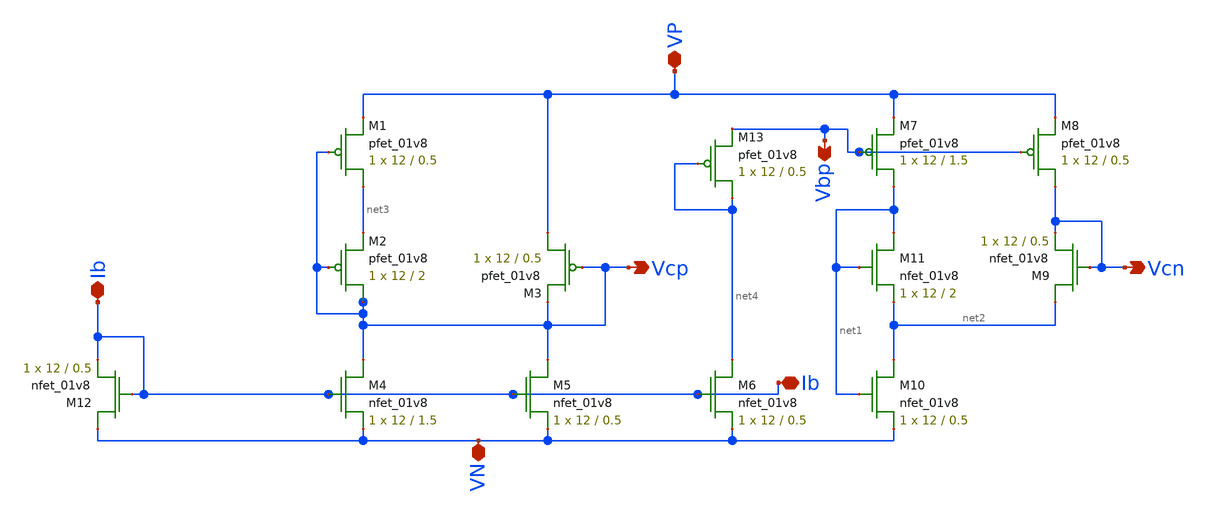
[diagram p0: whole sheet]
** sch_path: mp3/schematic/bias.sch
**.subckt bias VP VN Vcp Vcn Vbp Ib Ib
*.iopin VP
*.iopin VN
*.opin Vcp
*.opin Vcn
*.opin Vbp
*.iopin Ib
*.iopin Ib
XM1 net3 Vcp VP VDD sky130_fd_pr__pfet_01v8 L=0.5 W=12 nf=1 ad='int((nf+1)/2) * W/nf * 0.29' as='int((nf+2)/2) * W/nf * 0.29'
+ pd='2*int((nf+1)/2) * (W/nf + 0.29)' ps='2*int((nf+2)/2) * (W/nf + 0.29)' nrd='0.29 / W' nrs='0.29 / W'
+ sa=0 sb=0 sd=0 mult=1 m=1
XM2 Vcp Vcp net3 VDD sky130_fd_pr__pfet_01v8 L=2 W=12 nf=1 ad='int((nf+1)/2) * W/nf * 0.29' as='int((nf+2)/2) * W/nf * 0.29'
+ pd='2*int((nf+1)/2) * (W/nf + 0.29)' ps='2*int((nf+2)/2) * (W/nf + 0.29)' nrd='0.29 / W' nrs='0.29 / W'
+ sa=0 sb=0 sd=0 mult=1 m=1
XM3 VP Vcp Vcp VDD sky130_fd_pr__pfet_01v8 L=0.5 W=12 nf=1 ad='int((nf+1)/2) * W/nf * 0.29' as='int((nf+2)/2) * W/nf * 0.29'
+ pd='2*int((nf+1)/2) * (W/nf + 0.29)' ps='2*int((nf+2)/2) * (W/nf + 0.29)' nrd='0.29 / W' nrs='0.29 / W'
+ sa=0 sb=0 sd=0 mult=1 m=1
XM4 Vcp Ib VN GND sky130_fd_pr__nfet_01v8 L=1.5 W=12 nf=1 ad='int((nf+1)/2) * W/nf * 0.29' as='int((nf+2)/2) * W/nf * 0.29'
+ pd='2*int((nf+1)/2) * (W/nf + 0.29)' ps='2*int((nf+2)/2) * (W/nf + 0.29)' nrd='0.29 / W' nrs='0.29 / W'
+ sa=0 sb=0 sd=0 mult=1 m=1
XM5 Vcp Ib VN GND sky130_fd_pr__nfet_01v8 L=0.5 W=12 nf=1 ad='int((nf+1)/2) * W/nf * 0.29' as='int((nf+2)/2) * W/nf * 0.29'
+ pd='2*int((nf+1)/2) * (W/nf + 0.29)' ps='2*int((nf+2)/2) * (W/nf + 0.29)' nrd='0.29 / W' nrs='0.29 / W'
+ sa=0 sb=0 sd=0 mult=1 m=1
XM6 net4 Ib VN GND sky130_fd_pr__nfet_01v8 L=0.5 W=12 nf=1 ad='int((nf+1)/2) * W/nf * 0.29' as='int((nf+2)/2) * W/nf * 0.29'
+ pd='2*int((nf+1)/2) * (W/nf + 0.29)' ps='2*int((nf+2)/2) * (W/nf + 0.29)' nrd='0.29 / W' nrs='0.29 / W'
+ sa=0 sb=0 sd=0 mult=1 m=1
XM7 net1 Vbp VP VDD sky130_fd_pr__pfet_01v8 L=1.5 W=12 nf=1 ad='int((nf+1)/2) * W/nf * 0.29' as='int((nf+2)/2) * W/nf * 0.29'
+ pd='2*int((nf+1)/2) * (W/nf + 0.29)' ps='2*int((nf+2)/2) * (W/nf + 0.29)' nrd='0.29 / W' nrs='0.29 / W'
+ sa=0 sb=0 sd=0 mult=1 m=1
XM8 Vcn Vbp VP VDD sky130_fd_pr__pfet_01v8 L=0.5 W=12 nf=1 ad='int((nf+1)/2) * W/nf * 0.29' as='int((nf+2)/2) * W/nf * 0.29'
+ pd='2*int((nf+1)/2) * (W/nf + 0.29)' ps='2*int((nf+2)/2) * (W/nf + 0.29)' nrd='0.29 / W' nrs='0.29 / W'
+ sa=0 sb=0 sd=0 mult=1 m=1
XM9 net2 Vcn Vcn GND sky130_fd_pr__nfet_01v8 L=0.5 W=12 nf=1 ad='int((nf+1)/2) * W/nf * 0.29' as='int((nf+2)/2) * W/nf * 0.29'
+ pd='2*int((nf+1)/2) * (W/nf + 0.29)' ps='2*int((nf+2)/2) * (W/nf + 0.29)' nrd='0.29 / W' nrs='0.29 / W'
+ sa=0 sb=0 sd=0 mult=1 m=1
XM10 net2 net1 VN GND sky130_fd_pr__nfet_01v8 L=0.5 W=12 nf=1 ad='int((nf+1)/2) * W/nf * 0.29' as='int((nf+2)/2) * W/nf * 0.29'
+ pd='2*int((nf+1)/2) * (W/nf + 0.29)' ps='2*int((nf+2)/2) * (W/nf + 0.29)' nrd='0.29 / W' nrs='0.29 / W'
+ sa=0 sb=0 sd=0 mult=1 m=1
XM11 net1 net1 net2 GND sky130_fd_pr__nfet_01v8 L=2 W=12 nf=1 ad='int((nf+1)/2) * W/nf * 0.29' as='int((nf+2)/2) * W/nf * 0.29'
+ pd='2*int((nf+1)/2) * (W/nf + 0.29)' ps='2*int((nf+2)/2) * (W/nf + 0.29)' nrd='0.29 / W' nrs='0.29 / W'
+ sa=0 sb=0 sd=0 mult=1 m=1
XM12 VN Ib Ib GND sky130_fd_pr__nfet_01v8 L=0.5 W=12 nf=1 ad='int((nf+1)/2) * W/nf * 0.29' as='int((nf+2)/2) * W/nf * 0.29'
+ pd='2*int((nf+1)/2) * (W/nf + 0.29)' ps='2*int((nf+2)/2) * (W/nf + 0.29)' nrd='0.29 / W' nrs='0.29 / W'
+ sa=0 sb=0 sd=0 mult=1 m=1
XM13 net4 net4 Vbp VDD sky130_fd_pr__pfet_01v8 L=0.5 W=12 nf=1 ad='int((nf+1)/2) * W/nf * 0.29' as='int((nf+2)/2) * W/nf * 0.29'
+ pd='2*int((nf+1)/2) * (W/nf + 0.29)' ps='2*int((nf+2)/2) * (W/nf + 0.29)' nrd='0.29 / W' nrs='0.29 / W'
+ sa=0 sb=0 sd=0 mult=1 m=1
**.ends
.end
